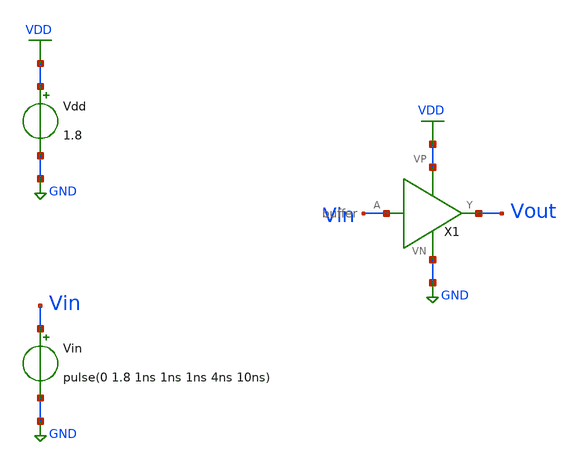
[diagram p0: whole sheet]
** sch_path: projects/inverter_tutorial/xschem_ngspice/buffer_tran.sch
**.subckt buffer_tran
Vdd VDD GND 1.8
Vin Vin GND pulse(0 1.8 1ns 1ns 1ns 4ns 10ns)
X1 Vin Vout VDD GND buffer
**** begin user architecture code



.lib /foss/pdks/sky130A/libs.tech/ngspice/sky130.lib.spice tt

.tran 0.01n 1u

.save all




**** end user architecture code
**.ends

* expanding   symbol:  /foss/designs/my_design/projects/inverter_tutorial/xschem_ngspice/buffer.sym
*+ # of pins=4
** sym_path: projects/inverter_tutorial/xschem_ngspice/buffer.sym
** sch_path: projects/inverter_tutorial/xschem_ngspice/buffer.sch
.subckt buffer A Y VP VN
*.ipin A
*.iopin VP
*.iopin VN
*.opin Y
X1 A net1 VP VN inverter
X2 net1 Y VP VN inverter
.ends


* expanding   symbol:
*+  /foss/designs/my_design/projects/inverter_tutorial/xschem_ngspice/inverter.sym # of pins=4
** sym_path: projects/inverter_tutorial/xschem_ngspice/inverter.sym
** sch_path: projects/inverter_tutorial/xschem_ngspice/inverter.sch
.subckt inverter A Y VP VN
*.ipin A
*.iopin VP
*.iopin VN
*.opin Y
XM1 Y A VN VN sky130_fd_pr__nfet_01v8 L=0.15 W=1 nf=1 ad='int((nf+1)/2) * W/nf * 0.29' as='int((nf+2)/2) * W/nf * 0.29'
+ pd='2*int((nf+1)/2) * (W/nf + 0.29)' ps='2*int((nf+2)/2) * (W/nf + 0.29)' nrd='0.29 / W' nrs='0.29 / W'
+ sa=0 sb=0 sd=0 mult=1 m=1
XM2 Y A VP VP sky130_fd_pr__pfet_01v8 L=0.15 W=1 nf=1 ad='int((nf+1)/2) * W/nf * 0.29' as='int((nf+2)/2) * W/nf * 0.29'
+ pd='2*int((nf+1)/2) * (W/nf + 0.29)' ps='2*int((nf+2)/2) * (W/nf + 0.29)' nrd='0.29 / W' nrs='0.29 / W'
+ sa=0 sb=0 sd=0 mult=1 m=1
.ends

.GLOBAL VDD
.GLOBAL GND
.end
